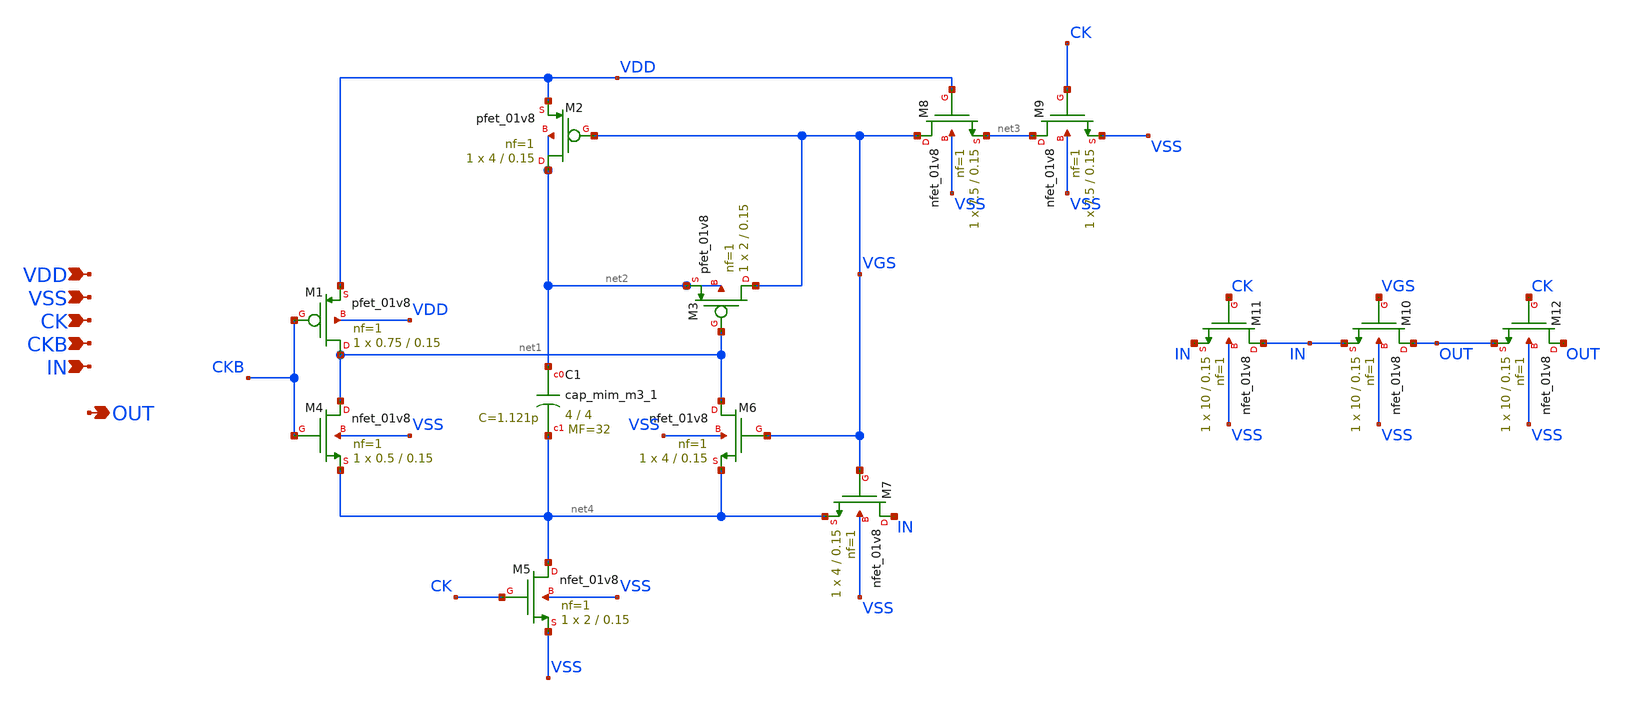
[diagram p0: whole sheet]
** sch_path: xschem/th_sw.sch
**.subckt th_sw VDD VSS CK CKB IN OUT
*.ipin VDD
*.ipin VSS
*.ipin CK
*.ipin CKB
*.ipin IN
*.opin OUT
XM1 net1 CKB VDD VDD sky130_fd_pr__pfet_01v8 L=0.15 W=0.75 nf=1 ad='int((nf+1)/2) * W/nf * 0.29' as='int((nf+2)/2) * W/nf * 0.29'
+ pd='2*int((nf+1)/2) * (W/nf + 0.29)' ps='2*int((nf+2)/2) * (W/nf + 0.29)' nrd='0.29 / W' nrs='0.29 / W'
+ sa=0 sb=0 sd=0 mult=1 m=1
XM2 net2 VGS VDD net2 sky130_fd_pr__pfet_01v8 L=0.15 W=4 nf=1 ad='int((nf+1)/2) * W/nf * 0.29' as='int((nf+2)/2) * W/nf * 0.29'
+ pd='2*int((nf+1)/2) * (W/nf + 0.29)' ps='2*int((nf+2)/2) * (W/nf + 0.29)' nrd='0.29 / W' nrs='0.29 / W'
+ sa=0 sb=0 sd=0 mult=1 m=1
XM3 VGS net1 net2 net2 sky130_fd_pr__pfet_01v8 L=0.15 W=2 nf=1 ad='int((nf+1)/2) * W/nf * 0.29' as='int((nf+2)/2) * W/nf * 0.29'
+ pd='2*int((nf+1)/2) * (W/nf + 0.29)' ps='2*int((nf+2)/2) * (W/nf + 0.29)' nrd='0.29 / W' nrs='0.29 / W'
+ sa=0 sb=0 sd=0 mult=1 m=1
XM4 net1 CKB net4 VSS sky130_fd_pr__nfet_01v8 L=0.15 W=0.5 nf=1 ad='int((nf+1)/2) * W/nf * 0.29' as='int((nf+2)/2) * W/nf * 0.29'
+ pd='2*int((nf+1)/2) * (W/nf + 0.29)' ps='2*int((nf+2)/2) * (W/nf + 0.29)' nrd='0.29 / W' nrs='0.29 / W'
+ sa=0 sb=0 sd=0 mult=1 m=1
XM5 net4 CK VSS VSS sky130_fd_pr__nfet_01v8 L=0.15 W=2 nf=1 ad='int((nf+1)/2) * W/nf * 0.29' as='int((nf+2)/2) * W/nf * 0.29'
+ pd='2*int((nf+1)/2) * (W/nf + 0.29)' ps='2*int((nf+2)/2) * (W/nf + 0.29)' nrd='0.29 / W' nrs='0.29 / W'
+ sa=0 sb=0 sd=0 mult=1 m=1
XM6 net1 VGS net4 VSS sky130_fd_pr__nfet_01v8 L=0.15 W=4 nf=1 ad='int((nf+1)/2) * W/nf * 0.29' as='int((nf+2)/2) * W/nf * 0.29'
+ pd='2*int((nf+1)/2) * (W/nf + 0.29)' ps='2*int((nf+2)/2) * (W/nf + 0.29)' nrd='0.29 / W' nrs='0.29 / W'
+ sa=0 sb=0 sd=0 mult=1 m=1
XM7 IN VGS net4 VSS sky130_fd_pr__nfet_01v8 L=0.15 W=4 nf=1 ad='int((nf+1)/2) * W/nf * 0.29' as='int((nf+2)/2) * W/nf * 0.29'
+ pd='2*int((nf+1)/2) * (W/nf + 0.29)' ps='2*int((nf+2)/2) * (W/nf + 0.29)' nrd='0.29 / W' nrs='0.29 / W'
+ sa=0 sb=0 sd=0 mult=1 m=1
XM8 VGS VDD net3 VSS sky130_fd_pr__nfet_01v8 L=0.15 W=7.5 nf=1 ad='int((nf+1)/2) * W/nf * 0.29' as='int((nf+2)/2) * W/nf * 0.29'
+ pd='2*int((nf+1)/2) * (W/nf + 0.29)' ps='2*int((nf+2)/2) * (W/nf + 0.29)' nrd='0.29 / W' nrs='0.29 / W'
+ sa=0 sb=0 sd=0 mult=1 m=1
XM9 net3 CK VSS VSS sky130_fd_pr__nfet_01v8 L=0.15 W=7.5 nf=1 ad='int((nf+1)/2) * W/nf * 0.29' as='int((nf+2)/2) * W/nf * 0.29'
+ pd='2*int((nf+1)/2) * (W/nf + 0.29)' ps='2*int((nf+2)/2) * (W/nf + 0.29)' nrd='0.29 / W' nrs='0.29 / W'
+ sa=0 sb=0 sd=0 mult=1 m=1
XC1 net2 net4 sky130_fd_pr__cap_mim_m3_1 W=4 L=4 MF=32 m=32
XM10 OUT VGS IN VSS sky130_fd_pr__nfet_01v8 L=0.15 W=10 nf=1 ad='int((nf+1)/2) * W/nf * 0.29' as='int((nf+2)/2) * W/nf * 0.29'
+ pd='2*int((nf+1)/2) * (W/nf + 0.29)' ps='2*int((nf+2)/2) * (W/nf + 0.29)' nrd='0.29 / W' nrs='0.29 / W'
+ sa=0 sb=0 sd=0 mult=1 m=1
XM11 IN CK IN VSS sky130_fd_pr__nfet_01v8 L=0.15 W=10 nf=1 ad='int((nf+1)/2) * W/nf * 0.29' as='int((nf+2)/2) * W/nf * 0.29'
+ pd='2*int((nf+1)/2) * (W/nf + 0.29)' ps='2*int((nf+2)/2) * (W/nf + 0.29)' nrd='0.29 / W' nrs='0.29 / W'
+ sa=0 sb=0 sd=0 mult=1 m=1
XM12 OUT CK OUT VSS sky130_fd_pr__nfet_01v8 L=0.15 W=10 nf=1 ad='int((nf+1)/2) * W/nf * 0.29' as='int((nf+2)/2) * W/nf * 0.29'
+ pd='2*int((nf+1)/2) * (W/nf + 0.29)' ps='2*int((nf+2)/2) * (W/nf + 0.29)' nrd='0.29 / W' nrs='0.29 / W'
+ sa=0 sb=0 sd=0 mult=1 m=1
**.ends
.end
